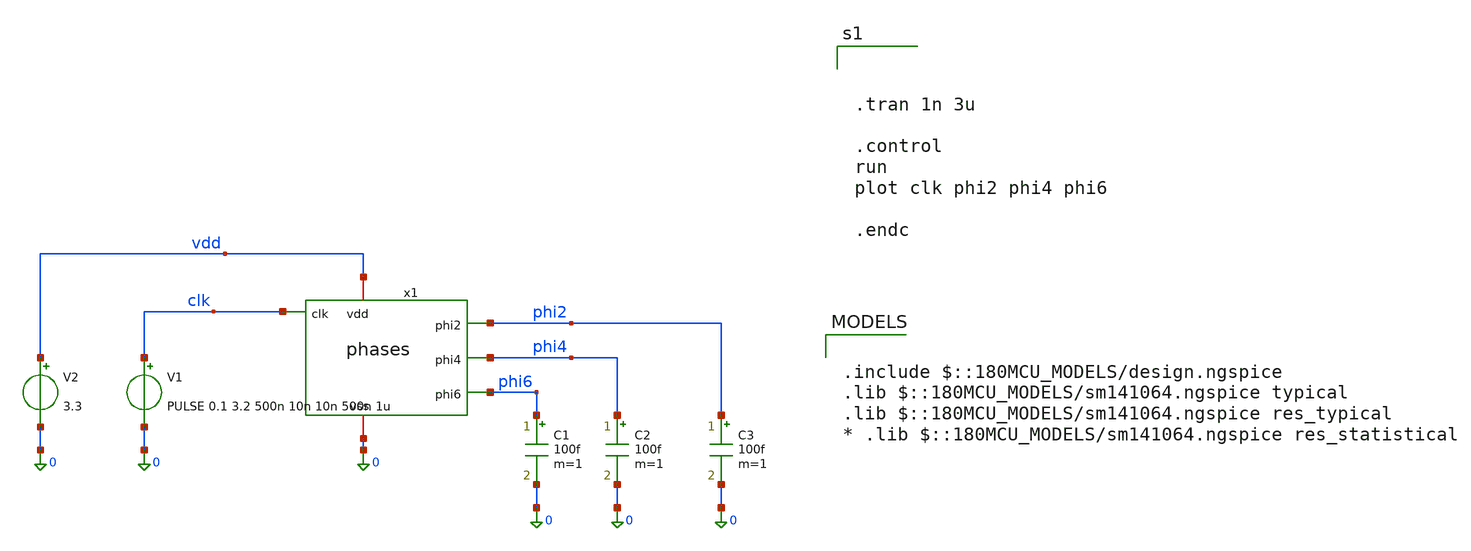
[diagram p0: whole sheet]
** sch_path: General/ADC/delay/phases_tb.sch
**.subckt phases_tb
V1 clk 0 PULSE 0.1 3.2 500n 10n 10n 500n 1u
x1 phi2 vdd phi4 clk phi6 0 phases
V2 vdd 0 3.3
C1 phi6 0 100f m=1
C2 phi4 0 100f m=1
C3 phi2 0 100f m=1
**** begin user architecture code

.include $::180MCU_MODELS/design.ngspice
.lib $::180MCU_MODELS/sm141064.ngspice typical
.lib $::180MCU_MODELS/sm141064.ngspice res_typical
* .lib $::180MCU_MODELS/sm141064.ngspice res_statistical




.tran 1n 3u

.control
run
plot clk phi2 phi4 phi6

.endc



**** end user architecture code
**.ends

* expanding   symbol:  ADC/delay/phases.sym # of pins=6
** sym_path: General/ADC/delay/phases.sym
** sch_path: General/ADC/delay/phases.sch
.subckt phases phi2 vdd phi4 clk phi6 vss
*.ipin clk
*.opin phi2
*.iopin vdd
*.iopin vss
*.opin phi4
*.opin phi6
x1 vdd clk phi2 vss delay
x2 vdd phi4 net1 vss clk and
x3 vdd phi2 net1 vss delay
x4 vdd phi6 phi2 vss clk or
.ends


* expanding   symbol:  ADC/delay/delay.sym # of pins=4
** sym_path: General/ADC/delay/delay.sym
** sch_path: General/ADC/delay/delay.sch
.subckt delay vdd A Y vss
*.ipin A
*.opin Y
*.iopin vdd
*.iopin vss
XM1 net1 A vss vss nfet_03v3 L=5u W=1u nf=1 ad='int((nf+1)/2) * W/nf * 0.18u' as='int((nf+2)/2) * W/nf * 0.18u'
+ pd='2*int((nf+1)/2) * (W/nf + 0.18u)' ps='2*int((nf+2)/2) * (W/nf + 0.18u)' nrd='0.18u / W' nrs='0.18u / W'
+ sa=0 sb=0 sd=0 m=1
XM3 net1 A vdd vdd pfet_03v3 L=5u W=2u nf=1 ad='int((nf+1)/2) * W/nf * 0.18u' as='int((nf+2)/2) * W/nf * 0.18u'
+ pd='2*int((nf+1)/2) * (W/nf + 0.18u)' ps='2*int((nf+2)/2) * (W/nf + 0.18u)' nrd='0.18u / W' nrs='0.18u / W'
+ sa=0 sb=0 sd=0 m=1
XM5 vdd net1 vdd vdd pfet_03v3 L=8u W=8u nf=1 ad='int((nf+1)/2) * W/nf * 0.18u' as='int((nf+2)/2) * W/nf * 0.18u'
+ pd='2*int((nf+1)/2) * (W/nf + 0.18u)' ps='2*int((nf+2)/2) * (W/nf + 0.18u)' nrd='0.18u / W' nrs='0.18u / W'
+ sa=0 sb=0 sd=0 m=1
XM6 vss net1 vss vss nfet_03v3 L=8u W=8u nf=1 ad='int((nf+1)/2) * W/nf * 0.18u' as='int((nf+2)/2) * W/nf * 0.18u'
+ pd='2*int((nf+1)/2) * (W/nf + 0.18u)' ps='2*int((nf+2)/2) * (W/nf + 0.18u)' nrd='0.18u / W' nrs='0.18u / W'
+ sa=0 sb=0 sd=0 m=1
XM7 net3 net2 vss vss nfet_03v3 L=2u W=1u nf=1 ad='int((nf+1)/2) * W/nf * 0.18u' as='int((nf+2)/2) * W/nf * 0.18u'
+ pd='2*int((nf+1)/2) * (W/nf + 0.18u)' ps='2*int((nf+2)/2) * (W/nf + 0.18u)' nrd='0.18u / W' nrs='0.18u / W'
+ sa=0 sb=0 sd=0 m=1
XM8 Y net3 vss vss nfet_03v3 L=0.28u W=5u nf=1 ad='int((nf+1)/2) * W/nf * 0.18u' as='int((nf+2)/2) * W/nf * 0.18u'
+ pd='2*int((nf+1)/2) * (W/nf + 0.18u)' ps='2*int((nf+2)/2) * (W/nf + 0.18u)' nrd='0.18u / W' nrs='0.18u / W'
+ sa=0 sb=0 sd=0 m=1
XM9 net3 net2 vdd vdd pfet_03v3 L=2u W=2u nf=1 ad='int((nf+1)/2) * W/nf * 0.18u' as='int((nf+2)/2) * W/nf * 0.18u'
+ pd='2*int((nf+1)/2) * (W/nf + 0.18u)' ps='2*int((nf+2)/2) * (W/nf + 0.18u)' nrd='0.18u / W' nrs='0.18u / W'
+ sa=0 sb=0 sd=0 m=1
XM10 Y net3 vdd vdd pfet_03v3 L=0.28u W=10u nf=1 ad='int((nf+1)/2) * W/nf * 0.18u' as='int((nf+2)/2) * W/nf * 0.18u'
+ pd='2*int((nf+1)/2) * (W/nf + 0.18u)' ps='2*int((nf+2)/2) * (W/nf + 0.18u)' nrd='0.18u / W' nrs='0.18u / W'
+ sa=0 sb=0 sd=0 m=1
XM11 vdd net2 vdd vdd pfet_03v3 L=8u W=8u nf=1 ad='int((nf+1)/2) * W/nf * 0.18u' as='int((nf+2)/2) * W/nf * 0.18u'
+ pd='2*int((nf+1)/2) * (W/nf + 0.18u)' ps='2*int((nf+2)/2) * (W/nf + 0.18u)' nrd='0.18u / W' nrs='0.18u / W'
+ sa=0 sb=0 sd=0 m=1
XM12 vss net2 vss vss nfet_03v3 L=8u W=8u nf=1 ad='int((nf+1)/2) * W/nf * 0.18u' as='int((nf+2)/2) * W/nf * 0.18u'
+ pd='2*int((nf+1)/2) * (W/nf + 0.18u)' ps='2*int((nf+2)/2) * (W/nf + 0.18u)' nrd='0.18u / W' nrs='0.18u / W'
+ sa=0 sb=0 sd=0 m=1
XM13 vdd net3 vdd vdd pfet_03v3 L=8u W=8u nf=1 ad='int((nf+1)/2) * W/nf * 0.18u' as='int((nf+2)/2) * W/nf * 0.18u'
+ pd='2*int((nf+1)/2) * (W/nf + 0.18u)' ps='2*int((nf+2)/2) * (W/nf + 0.18u)' nrd='0.18u / W' nrs='0.18u / W'
+ sa=0 sb=0 sd=0 m=1
XM14 vss net3 vss vss nfet_03v3 L=8u W=8u nf=1 ad='int((nf+1)/2) * W/nf * 0.18u' as='int((nf+2)/2) * W/nf * 0.18u'
+ pd='2*int((nf+1)/2) * (W/nf + 0.18u)' ps='2*int((nf+2)/2) * (W/nf + 0.18u)' nrd='0.18u / W' nrs='0.18u / W'
+ sa=0 sb=0 sd=0 m=1
XM2 net2 net1 vss vss nfet_03v3 L=5u W=1u nf=1 ad='int((nf+1)/2) * W/nf * 0.18u' as='int((nf+2)/2) * W/nf * 0.18u'
+ pd='2*int((nf+1)/2) * (W/nf + 0.18u)' ps='2*int((nf+2)/2) * (W/nf + 0.18u)' nrd='0.18u / W' nrs='0.18u / W'
+ sa=0 sb=0 sd=0 m=1
XM4 net2 net1 vdd vdd pfet_03v3 L=5u W=2u nf=1 ad='int((nf+1)/2) * W/nf * 0.18u' as='int((nf+2)/2) * W/nf * 0.18u'
+ pd='2*int((nf+1)/2) * (W/nf + 0.18u)' ps='2*int((nf+2)/2) * (W/nf + 0.18u)' nrd='0.18u / W' nrs='0.18u / W'
+ sa=0 sb=0 sd=0 m=1
.ends


* expanding   symbol:  ADC/delay/and.sym # of pins=5
** sym_path: General/ADC/delay/and.sym
** sch_path: General/ADC/delay/and.sch
.subckt and vdd Y A vss B
*.iopin vdd
*.iopin vss
*.ipin A
*.ipin B
*.opin Y
XM1 net1 B vss vss nfet_03v3 L=0.28u W=1u nf=1 ad='int((nf+1)/2) * W/nf * 0.18u' as='int((nf+2)/2) * W/nf * 0.18u'
+ pd='2*int((nf+1)/2) * (W/nf + 0.18u)' ps='2*int((nf+2)/2) * (W/nf + 0.18u)' nrd='0.18u / W' nrs='0.18u / W'
+ sa=0 sb=0 sd=0 m=1
XM2 net2 A net1 vss nfet_03v3 L=0.28u W=1u nf=1 ad='int((nf+1)/2) * W/nf * 0.18u' as='int((nf+2)/2) * W/nf * 0.18u'
+ pd='2*int((nf+1)/2) * (W/nf + 0.18u)' ps='2*int((nf+2)/2) * (W/nf + 0.18u)' nrd='0.18u / W' nrs='0.18u / W'
+ sa=0 sb=0 sd=0 m=1
XM3 Y net2 vss vss nfet_03v3 L=0.28u W=1u nf=1 ad='int((nf+1)/2) * W/nf * 0.18u' as='int((nf+2)/2) * W/nf * 0.18u'
+ pd='2*int((nf+1)/2) * (W/nf + 0.18u)' ps='2*int((nf+2)/2) * (W/nf + 0.18u)' nrd='0.18u / W' nrs='0.18u / W'
+ sa=0 sb=0 sd=0 m=1
XM4 net2 A vdd vdd pfet_03v3 L=0.28u W=2u nf=1 ad='int((nf+1)/2) * W/nf * 0.18u' as='int((nf+2)/2) * W/nf * 0.18u'
+ pd='2*int((nf+1)/2) * (W/nf + 0.18u)' ps='2*int((nf+2)/2) * (W/nf + 0.18u)' nrd='0.18u / W' nrs='0.18u / W'
+ sa=0 sb=0 sd=0 m=1
XM5 net2 B vdd vdd pfet_03v3 L=0.28u W=2u nf=1 ad='int((nf+1)/2) * W/nf * 0.18u' as='int((nf+2)/2) * W/nf * 0.18u'
+ pd='2*int((nf+1)/2) * (W/nf + 0.18u)' ps='2*int((nf+2)/2) * (W/nf + 0.18u)' nrd='0.18u / W' nrs='0.18u / W'
+ sa=0 sb=0 sd=0 m=1
XM6 Y net2 vdd vdd pfet_03v3 L=0.28u W=2u nf=1 ad='int((nf+1)/2) * W/nf * 0.18u' as='int((nf+2)/2) * W/nf * 0.18u'
+ pd='2*int((nf+1)/2) * (W/nf + 0.18u)' ps='2*int((nf+2)/2) * (W/nf + 0.18u)' nrd='0.18u / W' nrs='0.18u / W'
+ sa=0 sb=0 sd=0 m=1
.ends


* expanding   symbol:  ADC/delay/or.sym # of pins=5
** sym_path: General/ADC/delay/or.sym
** sch_path: General/ADC/delay/or.sch
.subckt or vdd Y A vss B
*.iopin vdd
*.iopin vss
*.ipin A
*.ipin B
*.opin Y
XM1 net1 B vss vss nfet_03v3 L=0.28u W=1u nf=1 ad='int((nf+1)/2) * W/nf * 0.18u' as='int((nf+2)/2) * W/nf * 0.18u'
+ pd='2*int((nf+1)/2) * (W/nf + 0.18u)' ps='2*int((nf+2)/2) * (W/nf + 0.18u)' nrd='0.18u / W' nrs='0.18u / W'
+ sa=0 sb=0 sd=0 m=1
XM2 net1 A vss vss nfet_03v3 L=0.28u W=1u nf=1 ad='int((nf+1)/2) * W/nf * 0.18u' as='int((nf+2)/2) * W/nf * 0.18u'
+ pd='2*int((nf+1)/2) * (W/nf + 0.18u)' ps='2*int((nf+2)/2) * (W/nf + 0.18u)' nrd='0.18u / W' nrs='0.18u / W'
+ sa=0 sb=0 sd=0 m=1
XM3 Y net1 vss vss nfet_03v3 L=0.28u W=1u nf=1 ad='int((nf+1)/2) * W/nf * 0.18u' as='int((nf+2)/2) * W/nf * 0.18u'
+ pd='2*int((nf+1)/2) * (W/nf + 0.18u)' ps='2*int((nf+2)/2) * (W/nf + 0.18u)' nrd='0.18u / W' nrs='0.18u / W'
+ sa=0 sb=0 sd=0 m=1
XM4 net2 A vdd vdd pfet_03v3 L=0.28u W=2u nf=1 ad='int((nf+1)/2) * W/nf * 0.18u' as='int((nf+2)/2) * W/nf * 0.18u'
+ pd='2*int((nf+1)/2) * (W/nf + 0.18u)' ps='2*int((nf+2)/2) * (W/nf + 0.18u)' nrd='0.18u / W' nrs='0.18u / W'
+ sa=0 sb=0 sd=0 m=1
XM5 net1 B net2 vdd pfet_03v3 L=0.28u W=2u nf=1 ad='int((nf+1)/2) * W/nf * 0.18u' as='int((nf+2)/2) * W/nf * 0.18u'
+ pd='2*int((nf+1)/2) * (W/nf + 0.18u)' ps='2*int((nf+2)/2) * (W/nf + 0.18u)' nrd='0.18u / W' nrs='0.18u / W'
+ sa=0 sb=0 sd=0 m=1
XM6 Y net1 vdd vdd pfet_03v3 L=0.28u W=2u nf=1 ad='int((nf+1)/2) * W/nf * 0.18u' as='int((nf+2)/2) * W/nf * 0.18u'
+ pd='2*int((nf+1)/2) * (W/nf + 0.18u)' ps='2*int((nf+2)/2) * (W/nf + 0.18u)' nrd='0.18u / W' nrs='0.18u / W'
+ sa=0 sb=0 sd=0 m=1
.ends

.end
